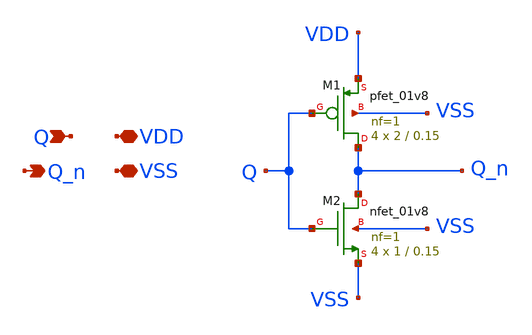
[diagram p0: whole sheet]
** sch_path: xschem/hello_world.sch
**.subckt hello_world Q Q_n VDD VSS
*.ipin Q
*.opin Q_n
*.iopin VDD
*.iopin VSS
XM1 Q_n Q VDD VSS sky130_fd_pr__pfet_01v8 L=0.15 W=2 nf=1 ad='int((nf+1)/2) * W/nf * 0.29' as='int((nf+2)/2) * W/nf * 0.29'
+ pd='2*int((nf+1)/2) * (W/nf + 0.29)' ps='2*int((nf+2)/2) * (W/nf + 0.29)' nrd='0.29 / W' nrs='0.29 / W'
+ sa=0 sb=0 sd=0 mult=4 m=4
XM2 Q_n Q VSS VSS sky130_fd_pr__nfet_01v8 L=0.15 W=1 nf=1 ad='int((nf+1)/2) * W/nf * 0.29' as='int((nf+2)/2) * W/nf * 0.29'
+ pd='2*int((nf+1)/2) * (W/nf + 0.29)' ps='2*int((nf+2)/2) * (W/nf + 0.29)' nrd='0.29 / W' nrs='0.29 / W'
+ sa=0 sb=0 sd=0 mult=4 m=4
**.ends
.end
